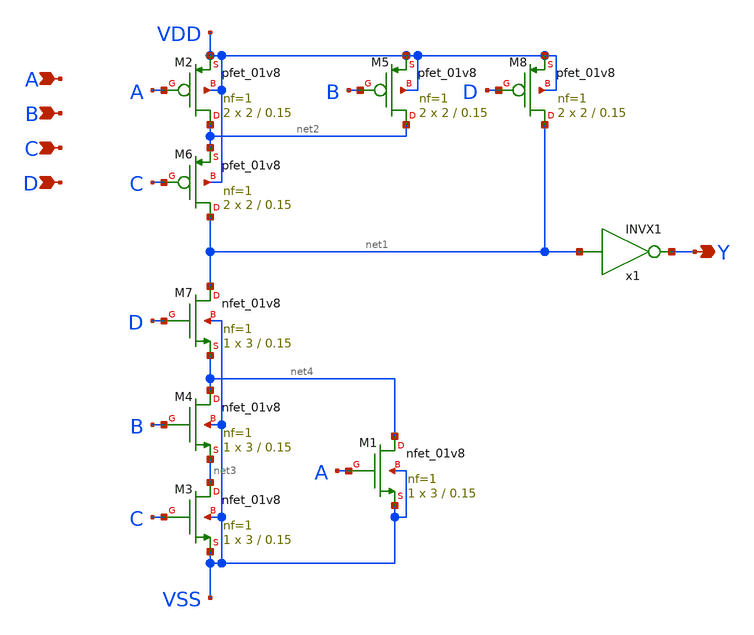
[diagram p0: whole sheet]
** sch_path: lib/xschem/AOA4X1.sch
**.subckt AOA4X1 Y A B C D
*.opin Y
*.ipin A
*.ipin B
*.ipin C
*.ipin D
XM1 net4 A VSS VSS sky130_fd_pr__nfet_01v8 L=0.15 W=3 nf=1 ad='int((nf+1)/2) * W/nf * 0.29' as='int((nf+2)/2) * W/nf * 0.29'
+ pd='2*int((nf+1)/2) * (W/nf + 0.29)' ps='2*int((nf+2)/2) * (W/nf + 0.29)' nrd='0.29 / W' nrs='0.29 / W'
+ sa=0 sb=0 sd=0 mult=1 m=1
XM2 net2 A VDD VDD sky130_fd_pr__pfet_01v8 L=0.15 W=2 nf=1 ad='int((nf+1)/2) * W/nf * 0.29' as='int((nf+2)/2) * W/nf * 0.29'
+ pd='2*int((nf+1)/2) * (W/nf + 0.29)' ps='2*int((nf+2)/2) * (W/nf + 0.29)' nrd='0.29 / W' nrs='0.29 / W'
+ sa=0 sb=0 sd=0 mult=2 m=2
XM3 net3 C VSS VSS sky130_fd_pr__nfet_01v8 L=0.15 W=3 nf=1 ad='int((nf+1)/2) * W/nf * 0.29' as='int((nf+2)/2) * W/nf * 0.29'
+ pd='2*int((nf+1)/2) * (W/nf + 0.29)' ps='2*int((nf+2)/2) * (W/nf + 0.29)' nrd='0.29 / W' nrs='0.29 / W'
+ sa=0 sb=0 sd=0 mult=1 m=1
XM4 net4 B net3 VSS sky130_fd_pr__nfet_01v8 L=0.15 W=3 nf=1 ad='int((nf+1)/2) * W/nf * 0.29' as='int((nf+2)/2) * W/nf * 0.29'
+ pd='2*int((nf+1)/2) * (W/nf + 0.29)' ps='2*int((nf+2)/2) * (W/nf + 0.29)' nrd='0.29 / W' nrs='0.29 / W'
+ sa=0 sb=0 sd=0 mult=1 m=1
XM5 net2 B VDD VDD sky130_fd_pr__pfet_01v8 L=0.15 W=2 nf=1 ad='int((nf+1)/2) * W/nf * 0.29' as='int((nf+2)/2) * W/nf * 0.29'
+ pd='2*int((nf+1)/2) * (W/nf + 0.29)' ps='2*int((nf+2)/2) * (W/nf + 0.29)' nrd='0.29 / W' nrs='0.29 / W'
+ sa=0 sb=0 sd=0 mult=2 m=2
XM6 net1 C net2 VDD sky130_fd_pr__pfet_01v8 L=0.15 W=2 nf=1 ad='int((nf+1)/2) * W/nf * 0.29' as='int((nf+2)/2) * W/nf * 0.29'
+ pd='2*int((nf+1)/2) * (W/nf + 0.29)' ps='2*int((nf+2)/2) * (W/nf + 0.29)' nrd='0.29 / W' nrs='0.29 / W'
+ sa=0 sb=0 sd=0 mult=2 m=2
x1 Y net1 INVX1
XM7 net1 D net4 VSS sky130_fd_pr__nfet_01v8 L=0.15 W=3 nf=1 ad='int((nf+1)/2) * W/nf * 0.29' as='int((nf+2)/2) * W/nf * 0.29'
+ pd='2*int((nf+1)/2) * (W/nf + 0.29)' ps='2*int((nf+2)/2) * (W/nf + 0.29)' nrd='0.29 / W' nrs='0.29 / W'
+ sa=0 sb=0 sd=0 mult=1 m=1
XM8 net1 D VDD VDD sky130_fd_pr__pfet_01v8 L=0.15 W=2 nf=1 ad='int((nf+1)/2) * W/nf * 0.29' as='int((nf+2)/2) * W/nf * 0.29'
+ pd='2*int((nf+1)/2) * (W/nf + 0.29)' ps='2*int((nf+2)/2) * (W/nf + 0.29)' nrd='0.29 / W' nrs='0.29 / W'
+ sa=0 sb=0 sd=0 mult=2 m=2
**.ends
.end
